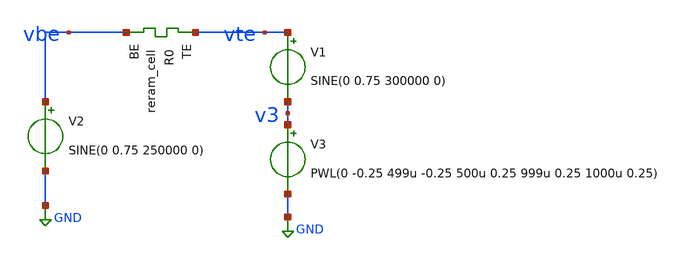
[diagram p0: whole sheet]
** sch_path: Synapse/syn_sine.sch
**.subckt syn_sine
XR0 vte vbe sky130_fd_pr_reram__reram_cell Tfilament_0=4.4e-9
V2 vbe GND SINE(0 0.75 250000 0)
V1 vte v3 SINE(0 0.75 300000 0)
V3 v3 GND PWL(0 -0.25 499u -0.25 500u 0.25 999u 0.25 1000u 0.25)
**** begin user architecture code

** opencircuitdesign pdks install
.inc $::SKYWATER_MODELS/sky130_fd_pr_reram__reram_cell.spice



.options savecurrents
.control
save all
tran 10n 1500u
write syn_sine.raw
.endc



**** end user architecture code
**.ends
.GLOBAL GND
.end
